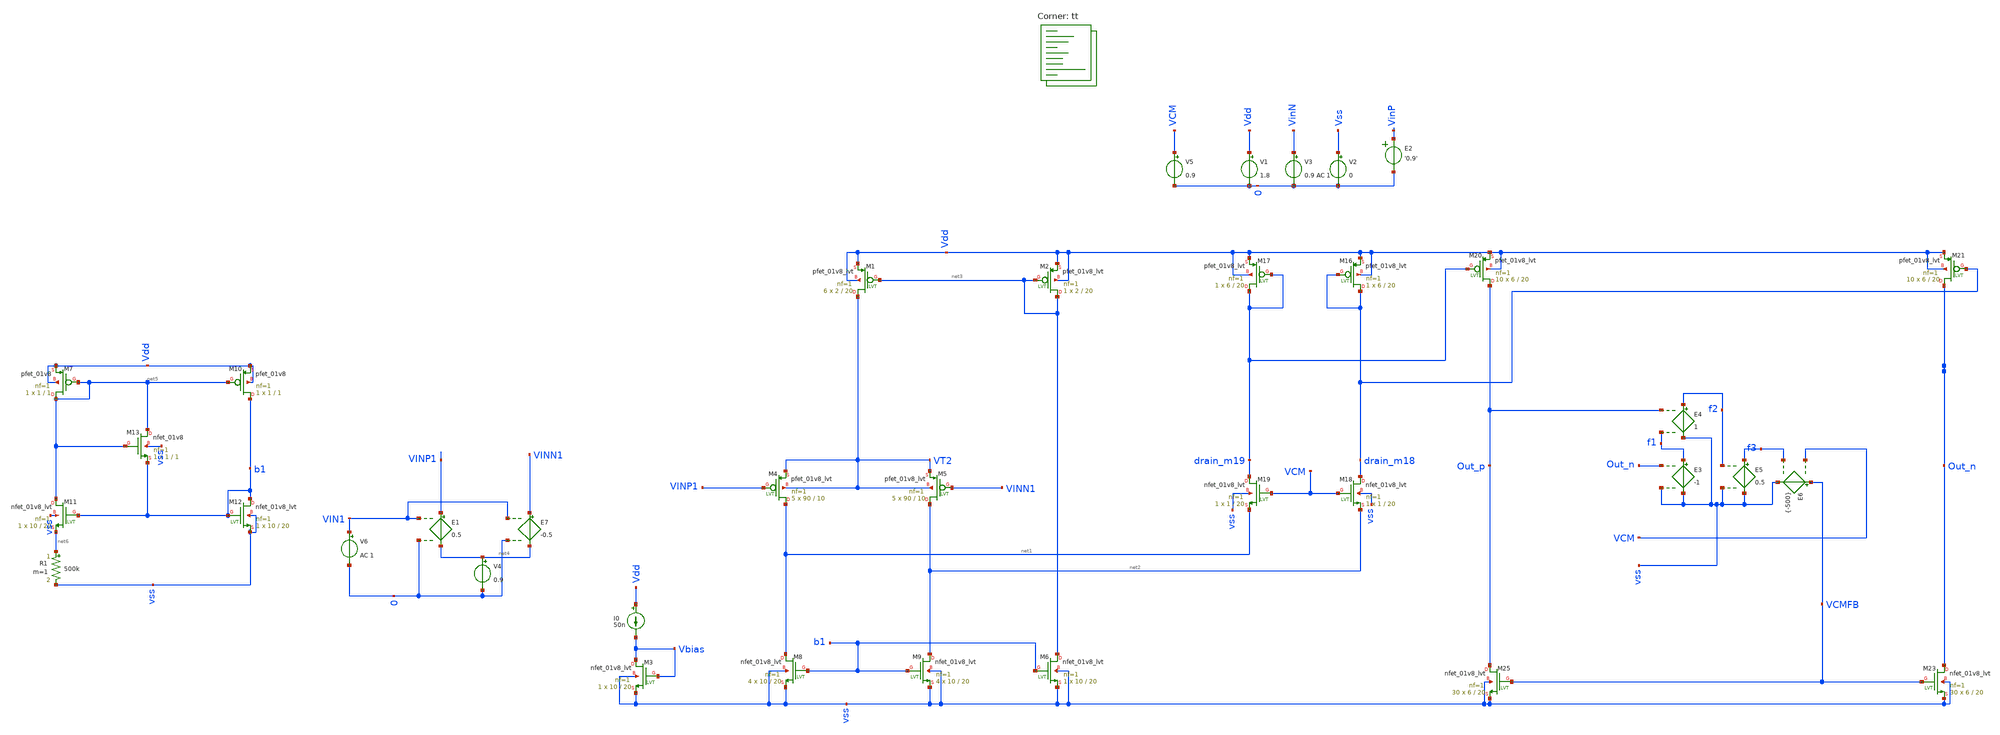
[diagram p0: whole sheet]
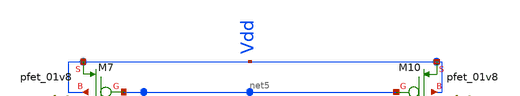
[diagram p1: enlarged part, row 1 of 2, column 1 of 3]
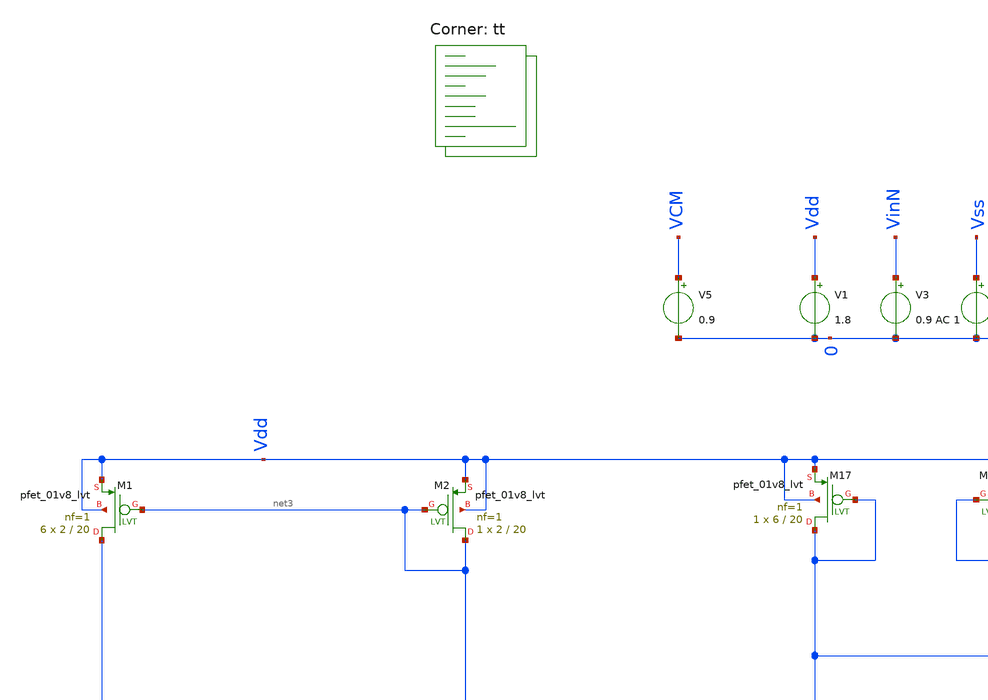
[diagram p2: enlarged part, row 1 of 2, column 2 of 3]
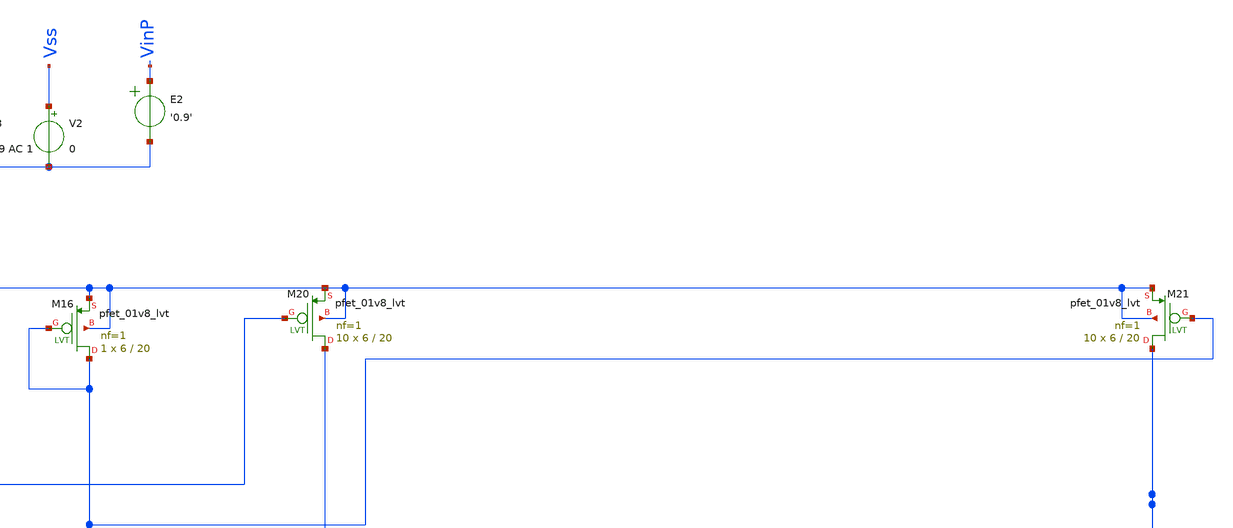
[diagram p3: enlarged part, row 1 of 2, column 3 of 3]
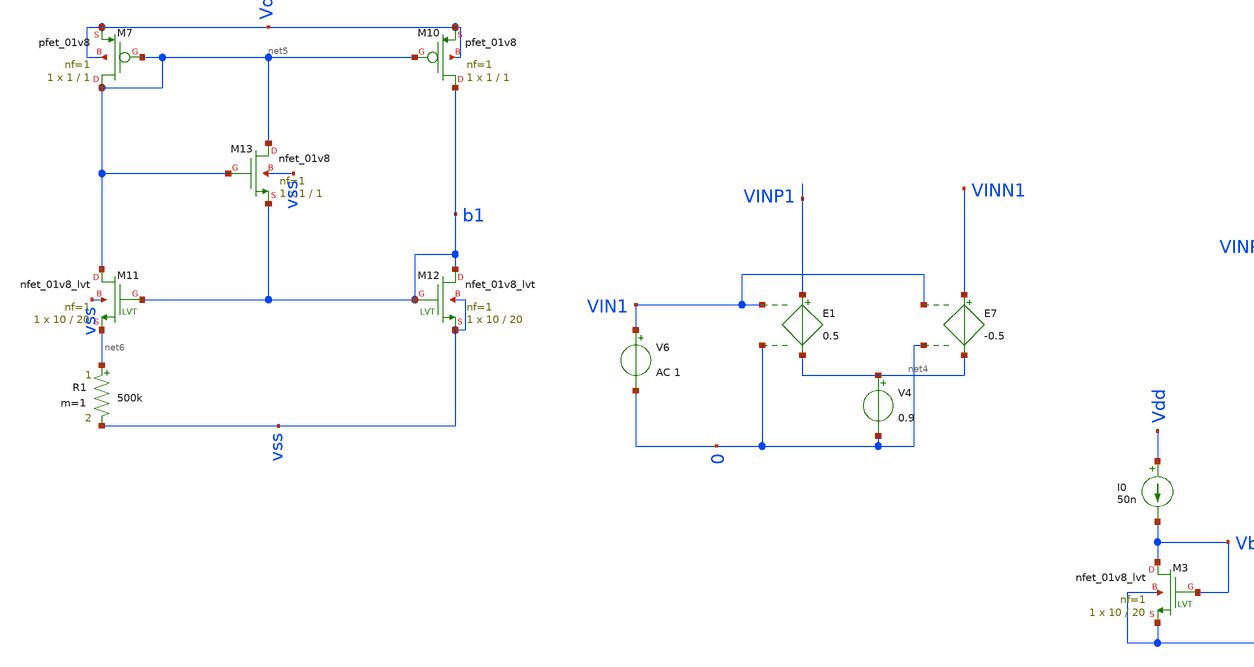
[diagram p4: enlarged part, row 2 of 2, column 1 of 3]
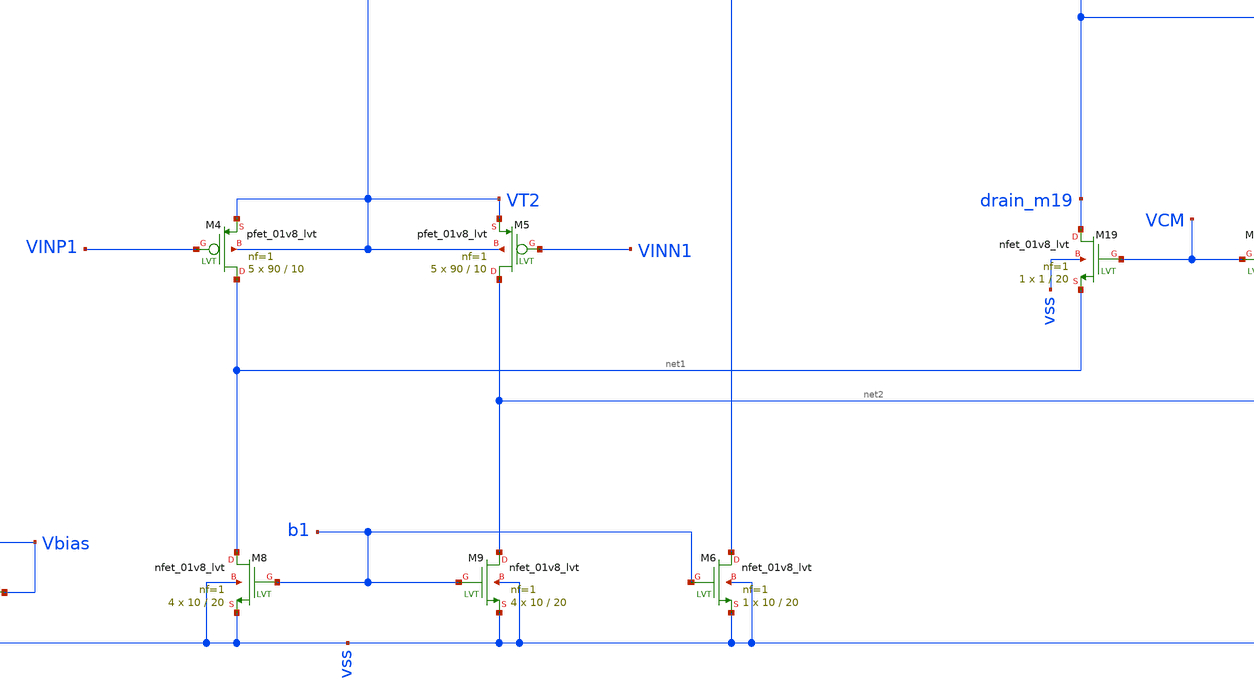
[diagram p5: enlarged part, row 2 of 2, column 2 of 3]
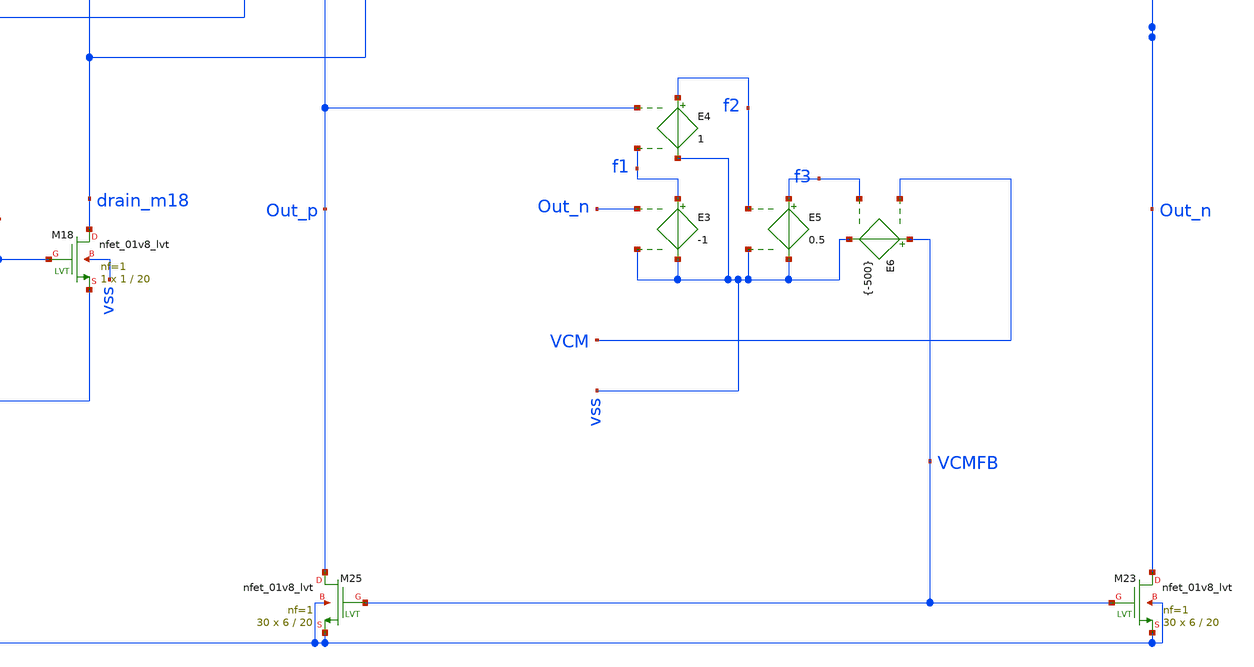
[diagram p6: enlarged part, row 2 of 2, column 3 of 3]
** sch_path: OL_noise.sch
**.subckt OL_noise
XM4 net1 VINP1 VT2 VT2 sky130_fd_pr__pfet_01v8_lvt L=10 W=90 nf=1 ad='int((nf+1)/2) * W/nf * 0.29' as='int((nf+2)/2) * W/nf * 0.29'
+ pd='2*int((nf+1)/2) * (W/nf + 0.29)' ps='2*int((nf+2)/2) * (W/nf + 0.29)' nrd='0.29 / W' nrs='0.29 / W'
+ sa=0 sb=0 sd=0 mult=5 m=5
XM5 net2 VINN1 VT2 VT2 sky130_fd_pr__pfet_01v8_lvt L=10 W=90 nf=1 ad='int((nf+1)/2) * W/nf * 0.29' as='int((nf+2)/2) * W/nf * 0.29'
+ pd='2*int((nf+1)/2) * (W/nf + 0.29)' ps='2*int((nf+2)/2) * (W/nf + 0.29)' nrd='0.29 / W' nrs='0.29 / W'
+ sa=0 sb=0 sd=0 mult=5 m=5
XM8 net1 b1 vss vss sky130_fd_pr__nfet_01v8_lvt L=20 W=10 nf=1 ad='int((nf+1)/2) * W/nf * 0.29' as='int((nf+2)/2) * W/nf * 0.29'
+ pd='2*int((nf+1)/2) * (W/nf + 0.29)' ps='2*int((nf+2)/2) * (W/nf + 0.29)' nrd='0.29 / W' nrs='0.29 / W'
+ sa=0 sb=0 sd=0 mult=4 m=4
XM9 net2 b1 vss vss sky130_fd_pr__nfet_01v8_lvt L=20 W=10 nf=1 ad='int((nf+1)/2) * W/nf * 0.29' as='int((nf+2)/2) * W/nf * 0.29'
+ pd='2*int((nf+1)/2) * (W/nf + 0.29)' ps='2*int((nf+2)/2) * (W/nf + 0.29)' nrd='0.29 / W' nrs='0.29 / W'
+ sa=0 sb=0 sd=0 mult=4 m=4
XM16 drain_m18 drain_m18 Vdd Vdd sky130_fd_pr__pfet_01v8_lvt L=20 W=6 nf=1 ad='int((nf+1)/2) * W/nf * 0.29'
+ as='int((nf+2)/2) * W/nf * 0.29' pd='2*int((nf+1)/2) * (W/nf + 0.29)' ps='2*int((nf+2)/2) * (W/nf + 0.29)'
+ nrd='0.29 / W' nrs='0.29 / W' sa=0 sb=0 sd=0 mult=1 m=1
XM17 drain_m19 drain_m19 Vdd Vdd sky130_fd_pr__pfet_01v8_lvt L=20 W=6 nf=1 ad='int((nf+1)/2) * W/nf * 0.29'
+ as='int((nf+2)/2) * W/nf * 0.29' pd='2*int((nf+1)/2) * (W/nf + 0.29)' ps='2*int((nf+2)/2) * (W/nf + 0.29)'
+ nrd='0.29 / W' nrs='0.29 / W' sa=0 sb=0 sd=0 mult=1 m=1
XM18 drain_m18 VCM net2 vss sky130_fd_pr__nfet_01v8_lvt L=20 W=1 nf=1 ad='int((nf+1)/2) * W/nf * 0.29'
+ as='int((nf+2)/2) * W/nf * 0.29' pd='2*int((nf+1)/2) * (W/nf + 0.29)' ps='2*int((nf+2)/2) * (W/nf + 0.29)'
+ nrd='0.29 / W' nrs='0.29 / W' sa=0 sb=0 sd=0 mult=1 m=1
XM19 drain_m19 VCM net1 vss sky130_fd_pr__nfet_01v8_lvt L=20 W=1 nf=1 ad='int((nf+1)/2) * W/nf * 0.29'
+ as='int((nf+2)/2) * W/nf * 0.29' pd='2*int((nf+1)/2) * (W/nf + 0.29)' ps='2*int((nf+2)/2) * (W/nf + 0.29)'
+ nrd='0.29 / W' nrs='0.29 / W' sa=0 sb=0 sd=0 mult=1 m=1
XM20 Out_p drain_m19 Vdd Vdd sky130_fd_pr__pfet_01v8_lvt L=20 W=6 nf=1 ad='int((nf+1)/2) * W/nf * 0.29'
+ as='int((nf+2)/2) * W/nf * 0.29' pd='2*int((nf+1)/2) * (W/nf + 0.29)' ps='2*int((nf+2)/2) * (W/nf + 0.29)'
+ nrd='0.29 / W' nrs='0.29 / W' sa=0 sb=0 sd=0 mult=10 m=10
XM21 Out_n drain_m18 Vdd Vdd sky130_fd_pr__pfet_01v8_lvt L=20 W=6 nf=1 ad='int((nf+1)/2) * W/nf * 0.29'
+ as='int((nf+2)/2) * W/nf * 0.29' pd='2*int((nf+1)/2) * (W/nf + 0.29)' ps='2*int((nf+2)/2) * (W/nf + 0.29)'
+ nrd='0.29 / W' nrs='0.29 / W' sa=0 sb=0 sd=0 mult=10 m=10
XM23 Out_n VCMFB vss vss sky130_fd_pr__nfet_01v8_lvt L=20 W=6 nf=1 ad='int((nf+1)/2) * W/nf * 0.29' as='int((nf+2)/2) * W/nf * 0.29'
+ pd='2*int((nf+1)/2) * (W/nf + 0.29)' ps='2*int((nf+2)/2) * (W/nf + 0.29)' nrd='0.29 / W' nrs='0.29 / W'
+ sa=0 sb=0 sd=0 mult=30 m=30
XM25 Out_p VCMFB vss vss sky130_fd_pr__nfet_01v8_lvt L=20 W=6 nf=1 ad='int((nf+1)/2) * W/nf * 0.29' as='int((nf+2)/2) * W/nf * 0.29'
+ pd='2*int((nf+1)/2) * (W/nf + 0.29)' ps='2*int((nf+2)/2) * (W/nf + 0.29)' nrd='0.29 / W' nrs='0.29 / W'
+ sa=0 sb=0 sd=0 mult=30 m=30
E2 VinP 0 VOL=' '0.9' '
V1 Vdd 0 1.8
V2 Vss 0 0
V5 VCM 0 0.9
XM1 VT2 net3 Vdd Vdd sky130_fd_pr__pfet_01v8_lvt L=20 W=2 nf=1 ad='int((nf+1)/2) * W/nf * 0.29' as='int((nf+2)/2) * W/nf * 0.29'
+ pd='2*int((nf+1)/2) * (W/nf + 0.29)' ps='2*int((nf+2)/2) * (W/nf + 0.29)' nrd='0.29 / W' nrs='0.29 / W'
+ sa=0 sb=0 sd=0 mult=6 m=6
XM2 net3 net3 Vdd Vdd sky130_fd_pr__pfet_01v8_lvt L=20 W=2 nf=1 ad='int((nf+1)/2) * W/nf * 0.29' as='int((nf+2)/2) * W/nf * 0.29'
+ pd='2*int((nf+1)/2) * (W/nf + 0.29)' ps='2*int((nf+2)/2) * (W/nf + 0.29)' nrd='0.29 / W' nrs='0.29 / W'
+ sa=0 sb=0 sd=0 mult=1 m=1
V3 VinN 0 0.9 AC 1
I0 Vdd Vbias 50n
XM3 Vbias Vbias vss vss sky130_fd_pr__nfet_01v8_lvt L=20 W=10 nf=1 ad='int((nf+1)/2) * W/nf * 0.29' as='int((nf+2)/2) * W/nf * 0.29'
+ pd='2*int((nf+1)/2) * (W/nf + 0.29)' ps='2*int((nf+2)/2) * (W/nf + 0.29)' nrd='0.29 / W' nrs='0.29 / W'
+ sa=0 sb=0 sd=0 mult=1 m=1
XM6 net3 b1 vss vss sky130_fd_pr__nfet_01v8_lvt L=20 W=10 nf=1 ad='int((nf+1)/2) * W/nf * 0.29' as='int((nf+2)/2) * W/nf * 0.29'
+ pd='2*int((nf+1)/2) * (W/nf + 0.29)' ps='2*int((nf+2)/2) * (W/nf + 0.29)' nrd='0.29 / W' nrs='0.29 / W'
+ sa=0 sb=0 sd=0 mult=1 m=1
E3 f1 vss Out_n vss -1
E4 f2 vss Out_p f1 1
E5 f3 vss f2 vss 0.5
E6 VCMFB vss VCM f3 {-500}
E1 VINP1 net4 VIN1 0 0.5
E7 VINN1 net4 VIN1 0 -0.5
V4 net4 0 0.9
V6 VIN1 0 AC 1
XM7 net5 net5 Vdd Vdd sky130_fd_pr__pfet_01v8 L=1 W=1 nf=1 ad='int((nf+1)/2) * W/nf * 0.29' as='int((nf+2)/2) * W/nf * 0.29'
+ pd='2*int((nf+1)/2) * (W/nf + 0.29)' ps='2*int((nf+2)/2) * (W/nf + 0.29)' nrd='0.29 / W' nrs='0.29 / W'
+ sa=0 sb=0 sd=0 mult=1 m=1
XM10 b1 net5 Vdd Vdd sky130_fd_pr__pfet_01v8 L=1 W=1 nf=1 ad='int((nf+1)/2) * W/nf * 0.29' as='int((nf+2)/2) * W/nf * 0.29'
+ pd='2*int((nf+1)/2) * (W/nf + 0.29)' ps='2*int((nf+2)/2) * (W/nf + 0.29)' nrd='0.29 / W' nrs='0.29 / W'
+ sa=0 sb=0 sd=0 mult=1 m=1
XM11 net5 b1 net6 vss sky130_fd_pr__nfet_01v8_lvt L=20 W=10 nf=1 ad='int((nf+1)/2) * W/nf * 0.29' as='int((nf+2)/2) * W/nf * 0.29'
+ pd='2*int((nf+1)/2) * (W/nf + 0.29)' ps='2*int((nf+2)/2) * (W/nf + 0.29)' nrd='0.29 / W' nrs='0.29 / W'
+ sa=0 sb=0 sd=0 mult=1 m=1
XM12 b1 b1 vss vss sky130_fd_pr__nfet_01v8_lvt L=20 W=10 nf=1 ad='int((nf+1)/2) * W/nf * 0.29' as='int((nf+2)/2) * W/nf * 0.29'
+ pd='2*int((nf+1)/2) * (W/nf + 0.29)' ps='2*int((nf+2)/2) * (W/nf + 0.29)' nrd='0.29 / W' nrs='0.29 / W'
+ sa=0 sb=0 sd=0 mult=1 m=1
XM13 net5 net5 b1 vss sky130_fd_pr__nfet_01v8 L=1 W=1 nf=1 ad='int((nf+1)/2) * W/nf * 0.29' as='int((nf+2)/2) * W/nf * 0.29'
+ pd='2*int((nf+1)/2) * (W/nf + 0.29)' ps='2*int((nf+2)/2) * (W/nf + 0.29)' nrd='0.29 / W' nrs='0.29 / W'
+ sa=0 sb=0 sd=0 mult=1 m=1
R1 net6 vss 500k m=1
**** begin user architecture code
.lib $::SKYWATER_MODELS/sky130.lib.spice tt


.options savecurrents
*ic v(VM5)=0.9 v(VM6)=0.9
.control


save all

save @m.xm11.msky130_fd_pr__pfet_01v8_lvt[id]
save @m.xm11.msky130_fd_pr__pfet_01v8_lvt[vgs]


*nmos
save @m.xm3.msky130_fd_pr__nfet_01v8_lvt[vgs]
save @m.xm3.msky130_fd_pr__nfet_01v8_lvt[vth]
save @m.xm3.msky130_fd_pr__nfet_01v8_lvt[vds]

save @m.xm6.msky130_fd_pr__nfet_01v8_lvt[vgs]
save @m.xm6.msky130_fd_pr__nfet_01v8_lvt[vth]
save @m.xm6.msky130_fd_pr__nfet_01v8_lvt[vds]

save @m.xm8.msky130_fd_pr__nfet_01v8_lvt[vgs]
save @m.xm8.msky130_fd_pr__nfet_01v8_lvt[vth]
save @m.xm8.msky130_fd_pr__nfet_01v8_lvt[vds]

save @m.xm9.msky130_fd_pr__nfet_01v8_lvt[vgs]
save @m.xm9.msky130_fd_pr__nfet_01v8_lvt[vth]
save @m.xm9.msky130_fd_pr__nfet_01v8_lvt[vds]

save @m.xm18.msky130_fd_pr__nfet_01v8_lvt[vgs]
save @m.xm18.msky130_fd_pr__nfet_01v8_lvt[vth]
save @m.xm18.msky130_fd_pr__nfet_01v8_lvt[vds]

save @m.xm19.msky130_fd_pr__nfet_01v8_lvt[vgs]
save @m.xm19.msky130_fd_pr__nfet_01v8_lvt[vth]
save @m.xm19.msky130_fd_pr__nfet_01v8_lvt[vds]

save @m.xm25.msky130_fd_pr__nfet_01v8_lvt[vgs]
save @m.xm25.msky130_fd_pr__nfet_01v8_lvt[vth]
save @m.xm25.msky130_fd_pr__nfet_01v8_lvt[vds]

*pmos

save @m.xm1.msky130_fd_pr__pfet_01v8_lvt[vgs]
save @m.xm1.msky130_fd_pr__pfet_01v8_lvt[vth]
save @m.xm1.msky130_fd_pr__pfet_01v8_lvt[vds]


save @m.xm2.msky130_fd_pr__pfet_01v8_lvt[vgs]
save @m.xm2.msky130_fd_pr__pfet_01v8_lvt[vth]
save @m.xm2.msky130_fd_pr__pfet_01v8_lvt[vds]


save @m.xm10.msky130_fd_pr__pfet_01v8_lvt[vgs]
save @m.xm10.msky130_fd_pr__pfet_01v8_lvt[vth]
save @m.xm10.msky130_fd_pr__pfet_01v8_lvt[vds]

save @m.xm13.msky130_fd_pr__pfet_01v8_lvt[vgs]
save @m.xm13.msky130_fd_pr__pfet_01v8_lvt[vth]
save @m.xm13.msky130_fd_pr__pfet_01v8_lvt[vds]

save @m.xm4.msky130_fd_pr__pfet_01v8_lvt[vgs]
save @m.xm4.msky130_fd_pr__pfet_01v8_lvt[vth]
save @m.xm4.msky130_fd_pr__pfet_01v8_lvt[vds]

save @m.xm5.msky130_fd_pr__pfet_01v8_lvt[vgs]
save @m.xm5.msky130_fd_pr__pfet_01v8_lvt[vth]
save @m.xm5.msky130_fd_pr__pfet_01v8_lvt[vds]

save @m.xm16.msky130_fd_pr__pfet_01v8_lvt[vgs]
save @m.xm16.msky130_fd_pr__pfet_01v8_lvt[vth]
save @m.xm16.msky130_fd_pr__pfet_01v8_lvt[vds]

save @m.xm17.msky130_fd_pr__pfet_01v8_lvt[vgs]
save @m.xm17.msky130_fd_pr__pfet_01v8_lvt[vth]
save @m.xm17.msky130_fd_pr__pfet_01v8_lvt[vds]

save @m.xm3.msky130_fd_pr__pfet_01v8_lvt[vgs]
save @m.xm3.msky130_fd_pr__pfet_01v8_lvt[vth]
save @m.xm3.msky130_fd_pr__pfet_01v8_lvt[vds]

save @m.xm20.msky130_fd_pr__pfet_01v8_lvt[vgs]
save @m.xm20.msky130_fd_pr__pfet_01v8_lvt[vth]
save @m.xm20.msky130_fd_pr__pfet_01v8_lvt[vds]

save @m.xm2.msky130_fd_pr__pfet_01v8_lvt[vgs]
save @m.xm2.msky130_fd_pr__pfet_01v8_lvt[vth]
save @m.xm2.msky130_fd_pr__pfet_01v8_lvt[vds]

save @m.xm21.msky130_fd_pr__pfet_01v8_lvt[vgs]
save @m.xm21.msky130_fd_pr__pfet_01v8_lvt[vth]
save @m.xm21.msky130_fd_pr__pfet_01v8_lvt[vds]

save @m.xm7.msky130_fd_pr__nfet_01v8_lvt[vth]

save @m.xm1.msky130_fd_pr__pfet_01v8[vgs]

save @m.xm1.msky130_fd_pr__nfet_01v8_lvt[gm]


save @m.xm1.msky130_fd_pr__nfet_01v8_lvt[gds]
save @m.xm2.msky130_fd_pr__pfet_01v8_lvt[gm]

save @m.xm23.msky130_fd_pr__nfet_01v8[cgs]
save @m.xm4.msky130_fd_pr__pfet_01v8[cgs]
save @m.xm2.msky130_fd_pr__pfet_01v8_lvt[cgs]



save @m.xm2.msky130_fd_pr__pfet_01v8_lvt[gds]


op
*remzerovec
write OL_noise.raw
*set appendwrite

*dc V1 0 1.8 0.01
*plot @m.xm1.msky130_fd_pr__nfet_01v8_lvt[id] @m.xm2.msky130_fd_pr__pfet_01v8_lvt[id]
*remzerovec
*write intro.raw

.endc
.control
let vth=@M.XM25.msky130_fd_pr__nfet_01v8_lvt[vgs]


noise V(Out_p,Out_n) V6 dec 100 0.1 128
print inoise_total onoise_total
setplot noise1
plot inoise_spectrum




tran 1n 1u
save all


ac dec 10 0.1 1k
let gaind=(v(out_p)-v(out_n))/(v(VINP1)-v(VINN1))
let gainc=(v(f3))/(v(f4))
plot db(gaind)
plot db(gaind/gainc)
.endc






.include $::SKYWATER_STDCELLS/sky130_fd_sc_hd.spice

**** end user architecture code
**.ends
.end
